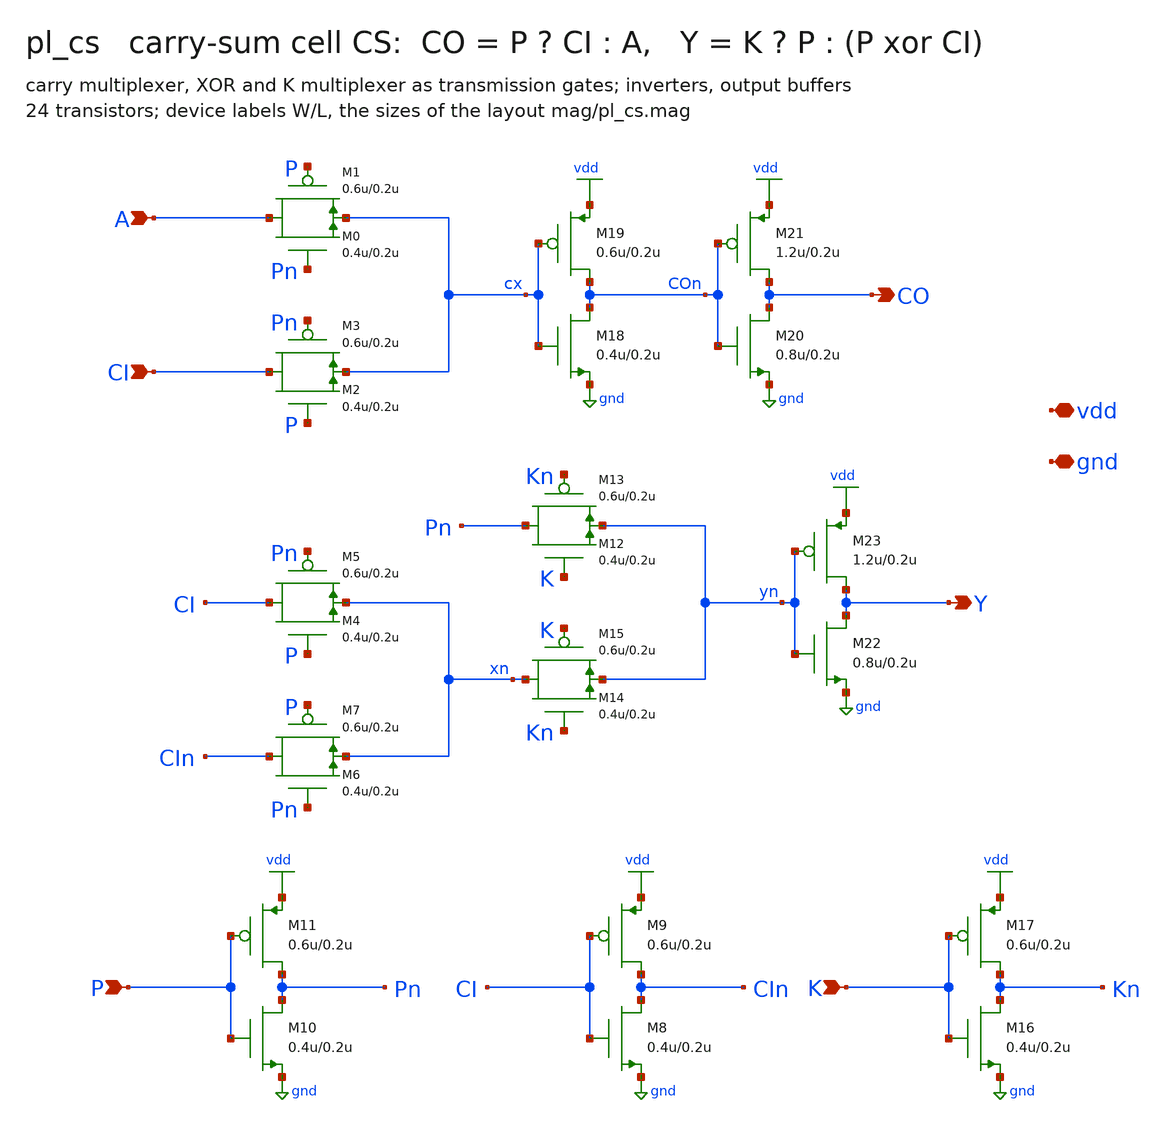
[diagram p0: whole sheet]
** sch_path: demo/xschem/pl_cs.sch
**.subckt pl_cs A CI CO Y P K vdd gnd
*.ipin A
*.ipin CI
*.opin CO
*.opin Y
*.ipin P
*.ipin K
*.iopin vdd
*.iopin gnd
M1 A P cx vdd pfet w=0.6u l=0.2u m=1
M0 A Pn cx gnd nfet w=0.4u l=0.2u m=1
M3 CI Pn cx vdd pfet w=0.6u l=0.2u m=1
M2 CI P cx gnd nfet w=0.4u l=0.2u m=1
M19 COn cx vdd vdd pfet w=0.6u l=0.2u m=1
M18 COn cx gnd gnd nfet w=0.4u l=0.2u m=1
M21 CO COn vdd vdd pfet w=1.2u l=0.2u m=1
M20 CO COn gnd gnd nfet w=0.8u l=0.2u m=1
M5 CI Pn xn vdd pfet w=0.6u l=0.2u m=1
M4 CI P xn gnd nfet w=0.4u l=0.2u m=1
M7 CIn P xn vdd pfet w=0.6u l=0.2u m=1
M6 CIn Pn xn gnd nfet w=0.4u l=0.2u m=1
M13 Pn Kn yn vdd pfet w=0.6u l=0.2u m=1
M12 Pn K yn gnd nfet w=0.4u l=0.2u m=1
M15 xn K yn vdd pfet w=0.6u l=0.2u m=1
M14 xn Kn yn gnd nfet w=0.4u l=0.2u m=1
M23 Y yn vdd vdd pfet w=1.2u l=0.2u m=1
M22 Y yn gnd gnd nfet w=0.8u l=0.2u m=1
M11 Pn P vdd vdd pfet w=0.6u l=0.2u m=1
M10 Pn P gnd gnd nfet w=0.4u l=0.2u m=1
M9 CIn CI vdd vdd pfet w=0.6u l=0.2u m=1
M8 CIn CI gnd gnd nfet w=0.4u l=0.2u m=1
M17 Kn K vdd vdd pfet w=0.6u l=0.2u m=1
M16 Kn K gnd gnd nfet w=0.4u l=0.2u m=1
**.ends
.GLOBAL vdd
.GLOBAL gnd
.end
